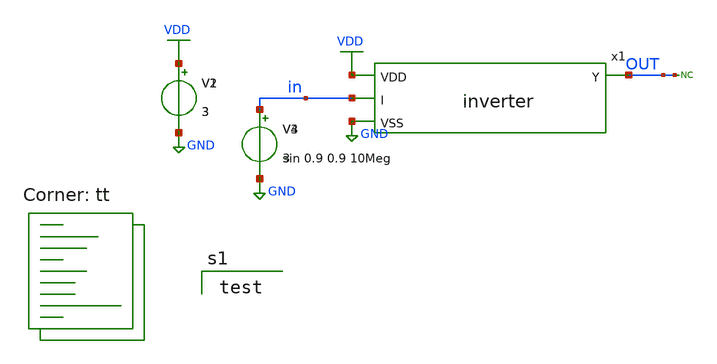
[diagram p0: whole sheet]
** sch_path: xschem/inv_tb.sch
**.subckt inv_tb
x1 VDD in OUT GND inverter
V1 VDD GND 3
V2 VDD GND 3
V3 in GND sin 0.9 0.9 10Meg
V4 in GND 3
* noconn OUT
**** begin user architecture code
.lib $::SKYWATER_MODELS/sky130.lib.spice tt

test


**** end user architecture code
**.ends

* expanding   symbol:  /home/ttuser/work/mixed_signal_chip/xschem/inverter.sym # of pins=4
** sym_path: xschem/inverter.sym
** sch_path: xschem/inverter.sch
.subckt inverter VDD I Y VSS
*.ipin I
*.ipin VDD
*.ipin VSS
*.opin Y
XM2 Y I VDD VDD sky130_fd_pr__pfet_01v8_lvt L=0.15 W=1 nf=1 ad='int((nf+1)/2) * W/nf * 0.29' as='int((nf+2)/2) * W/nf * 0.29'
+ pd='2*int((nf+1)/2) * (W/nf + 0.29)' ps='2*int((nf+2)/2) * (W/nf + 0.29)' nrd='0.29 / W' nrs='0.29 / W'
+ sa=0 sb=0 sd=0 mult=1 m=1
XM3 VSS I Y GND sky130_fd_pr__nfet_01v8_lvt L=0.15 W=1 nf=1 ad='int((nf+1)/2) * W/nf * 0.29' as='int((nf+2)/2) * W/nf * 0.29'
+ pd='2*int((nf+1)/2) * (W/nf + 0.29)' ps='2*int((nf+2)/2) * (W/nf + 0.29)' nrd='0.29 / W' nrs='0.29 / W'
+ sa=0 sb=0 sd=0 mult=1 m=1
.ends

.GLOBAL GND
.GLOBAL VDD
.end
